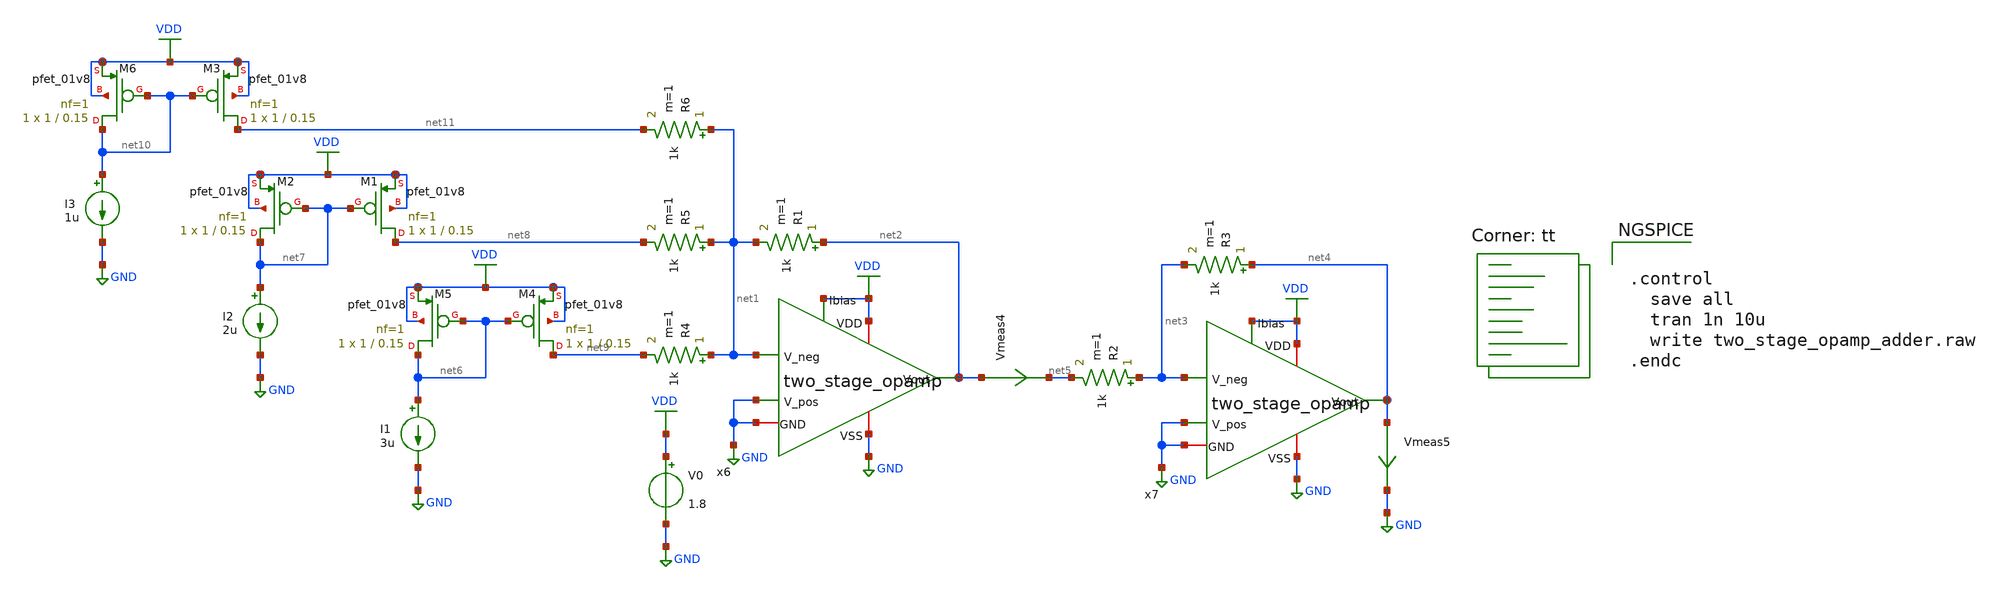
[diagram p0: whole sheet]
** sch_path: two_stage_opamp/two_stage_opamp_adder.sch
**.subckt two_stage_opamp_adder
x6 VDD net2 VDD net1 GND GND GND two_stage_opamp W1=15 W2=94 W3=3 W4=4.5 W5=14 W6=10 L1=0.15 L2=0.15
+ L3=0.15 L4=0.15 L5=0.15 L6=0.15
R1 net2 net1 1k m=1
R2 net3 net5 1k m=1
x7 VDD net4 VDD net3 GND GND GND two_stage_opamp W1=15 W2=94 W3=3 W4=4.5 W5=14 W6=10 L1=0.15 L2=0.15
+ L3=0.15 L4=0.15 L5=0.15 L6=0.15
R3 net4 net3 1k m=1
R4 net1 net9 1k m=1
R5 net1 net8 1k m=1
R6 net1 net11 1k m=1
V0 VDD GND 1.8
Vmeas4 net2 net5 0
.save i(vmeas4)
Vmeas5 net4 GND 0
.save i(vmeas5)
I1 net6 GND 3u
XM4 net9 net6 VDD VDD sky130_fd_pr__pfet_01v8 L=0.15 W=1 nf=1 ad='int((nf+1)/2) * W/nf * 0.29' as='int((nf+2)/2) * W/nf * 0.29'
+ pd='2*int((nf+1)/2) * (W/nf + 0.29)' ps='2*int((nf+2)/2) * (W/nf + 0.29)' nrd='0.29 / W' nrs='0.29 / W'
+ sa=0 sb=0 sd=0 mult=1 m=1
XM5 net6 net6 VDD VDD sky130_fd_pr__pfet_01v8 L=0.15 W=1 nf=1 ad='int((nf+1)/2) * W/nf * 0.29' as='int((nf+2)/2) * W/nf * 0.29'
+ pd='2*int((nf+1)/2) * (W/nf + 0.29)' ps='2*int((nf+2)/2) * (W/nf + 0.29)' nrd='0.29 / W' nrs='0.29 / W'
+ sa=0 sb=0 sd=0 mult=1 m=1
I2 net7 GND 2u
XM1 net8 net7 VDD VDD sky130_fd_pr__pfet_01v8 L=0.15 W=1 nf=1 ad='int((nf+1)/2) * W/nf * 0.29' as='int((nf+2)/2) * W/nf * 0.29'
+ pd='2*int((nf+1)/2) * (W/nf + 0.29)' ps='2*int((nf+2)/2) * (W/nf + 0.29)' nrd='0.29 / W' nrs='0.29 / W'
+ sa=0 sb=0 sd=0 mult=1 m=1
XM2 net7 net7 VDD VDD sky130_fd_pr__pfet_01v8 L=0.15 W=1 nf=1 ad='int((nf+1)/2) * W/nf * 0.29' as='int((nf+2)/2) * W/nf * 0.29'
+ pd='2*int((nf+1)/2) * (W/nf + 0.29)' ps='2*int((nf+2)/2) * (W/nf + 0.29)' nrd='0.29 / W' nrs='0.29 / W'
+ sa=0 sb=0 sd=0 mult=1 m=1
I3 net10 GND 1u
XM3 net11 net10 VDD VDD sky130_fd_pr__pfet_01v8 L=0.15 W=1 nf=1 ad='int((nf+1)/2) * W/nf * 0.29' as='int((nf+2)/2) * W/nf * 0.29'
+ pd='2*int((nf+1)/2) * (W/nf + 0.29)' ps='2*int((nf+2)/2) * (W/nf + 0.29)' nrd='0.29 / W' nrs='0.29 / W'
+ sa=0 sb=0 sd=0 mult=1 m=1
XM6 net10 net10 VDD VDD sky130_fd_pr__pfet_01v8 L=0.15 W=1 nf=1 ad='int((nf+1)/2) * W/nf * 0.29' as='int((nf+2)/2) * W/nf * 0.29'
+ pd='2*int((nf+1)/2) * (W/nf + 0.29)' ps='2*int((nf+2)/2) * (W/nf + 0.29)' nrd='0.29 / W' nrs='0.29 / W'
+ sa=0 sb=0 sd=0 mult=1 m=1
**** begin user architecture code
.lib $::SKYWATER_MODELS/sky130.lib.spice tt


.control
  save all
  tran 1n 10u
  write two_stage_opamp_adder.raw
.endc


**** end user architecture code
**.ends

* expanding   symbol:  /home/ricardo/RATT_repos/Proyectos_xschem/two_stage_opamp/two_stage_opamp.sym
*+ # of pins=7
** sym_path: two_stage_opamp/two_stage_opamp.sym
** sch_path: two_stage_opamp/two_stage_opamp.sch
.subckt two_stage_opamp VDD Vout Ibias V_neg GND V_pos VSS  W1=15 W2=94 W3=3 W4=4.5 W5=14 W6=10
+ L1=0.15 L2=0.15 L3=0.15 L4=0.15 L5=0.15 L6=0.15
*.ipin Ibias
*.ipin V_neg
*.ipin V_pos
*.iopin VDD
*.iopin VSS
*.opin Vout
*.iopin GND
XM1 net2 V_neg net4 VSS sky130_fd_pr__nfet_01v8 L=L3 W=W3 nf=1 ad='int((nf+1)/2) * W/nf * 0.29' as='int((nf+2)/2) * W/nf * 0.29'
+ pd='2*int((nf+1)/2) * (W/nf + 0.29)' ps='2*int((nf+2)/2) * (W/nf + 0.29)' nrd='0.29 / W' nrs='0.29 / W'
+ sa=0 sb=0 sd=0 mult=1 m=1
XM3 net2 net2 VDD VDD sky130_fd_pr__pfet_01v8 L=L1 W=W1 nf=1 ad='int((nf+1)/2) * W/nf * 0.29' as='int((nf+2)/2) * W/nf * 0.29'
+ pd='2*int((nf+1)/2) * (W/nf + 0.29)' ps='2*int((nf+2)/2) * (W/nf + 0.29)' nrd='0.29 / W' nrs='0.29 / W'
+ sa=0 sb=0 sd=0 mult=1 m=1
XM2 net3 V_pos net4 VSS sky130_fd_pr__nfet_01v8 L=L3 W=W3 nf=1 ad='int((nf+1)/2) * W/nf * 0.29' as='int((nf+2)/2) * W/nf * 0.29'
+ pd='2*int((nf+1)/2) * (W/nf + 0.29)' ps='2*int((nf+2)/2) * (W/nf + 0.29)' nrd='0.29 / W' nrs='0.29 / W'
+ sa=0 sb=0 sd=0 mult=1 m=1
XM4 net3 net2 VDD VDD sky130_fd_pr__pfet_01v8 L=L1 W=W1 nf=1 ad='int((nf+1)/2) * W/nf * 0.29' as='int((nf+2)/2) * W/nf * 0.29'
+ pd='2*int((nf+1)/2) * (W/nf + 0.29)' ps='2*int((nf+2)/2) * (W/nf + 0.29)' nrd='0.29 / W' nrs='0.29 / W'
+ sa=0 sb=0 sd=0 mult=1 m=1
XM5 net4 net1 VSS VSS sky130_fd_pr__nfet_01v8 L=L4 W=W4 nf=1 ad='int((nf+1)/2) * W/nf * 0.29' as='int((nf+2)/2) * W/nf * 0.29'
+ pd='2*int((nf+1)/2) * (W/nf + 0.29)' ps='2*int((nf+2)/2) * (W/nf + 0.29)' nrd='0.29 / W' nrs='0.29 / W'
+ sa=0 sb=0 sd=0 mult=1 m=1
XM6 Vout net3 VDD VDD sky130_fd_pr__pfet_01v8 L=L2 W=W2 nf=1 ad='int((nf+1)/2) * W/nf * 0.29' as='int((nf+2)/2) * W/nf * 0.29'
+ pd='2*int((nf+1)/2) * (W/nf + 0.29)' ps='2*int((nf+2)/2) * (W/nf + 0.29)' nrd='0.29 / W' nrs='0.29 / W'
+ sa=0 sb=0 sd=0 mult=1 m=1
XM7 Vout net1 VSS VSS sky130_fd_pr__nfet_01v8 L=L5 W=W5 nf=1 ad='int((nf+1)/2) * W/nf * 0.29' as='int((nf+2)/2) * W/nf * 0.29'
+ pd='2*int((nf+1)/2) * (W/nf + 0.29)' ps='2*int((nf+2)/2) * (W/nf + 0.29)' nrd='0.29 / W' nrs='0.29 / W'
+ sa=0 sb=0 sd=0 mult=1 m=1
XM8 net1 net1 VSS VSS sky130_fd_pr__nfet_01v8 L=L4 W=W4 nf=1 ad='int((nf+1)/2) * W/nf * 0.29' as='int((nf+2)/2) * W/nf * 0.29'
+ pd='2*int((nf+1)/2) * (W/nf + 0.29)' ps='2*int((nf+2)/2) * (W/nf + 0.29)' nrd='0.29 / W' nrs='0.29 / W'
+ sa=0 sb=0 sd=0 mult=1 m=1
XM9 net1 net1 Ibias Ibias sky130_fd_pr__pfet_01v8 L=L6 W=W6 nf=1 ad='int((nf+1)/2) * W/nf * 0.29' as='int((nf+2)/2) * W/nf * 0.29'
+ pd='2*int((nf+1)/2) * (W/nf + 0.29)' ps='2*int((nf+2)/2) * (W/nf + 0.29)' nrd='0.29 / W' nrs='0.29 / W'
+ sa=0 sb=0 sd=0 mult=1 m=1
XC1 net3 Vout sky130_fd_pr__cap_mim_m3_1 W=10 L=1 MF=1 m=1
.ends

.GLOBAL GND
.GLOBAL VDD
.end
